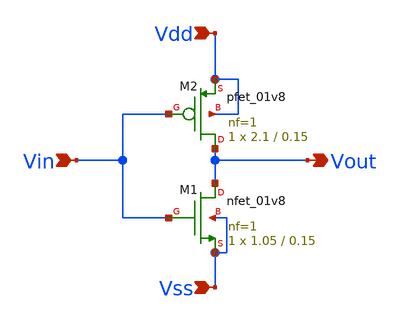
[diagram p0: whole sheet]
** sch_path: trabajosPracticos/tp6/archivosDelProfe/inversor/inversor.sch
**.subckt inversor Vdd Vss Vin Vout
*.ipin Vdd
*.ipin Vss
*.ipin Vin
*.opin Vout
XM2 Vout Vin Vdd Vdd sky130_fd_pr__pfet_01v8 L=0.15 W=2.1 nf=1 ad='int((nf+1)/2) * W/nf * 0.29' as='int((nf+2)/2) * W/nf * 0.29'
+ pd='2*int((nf+1)/2) * (W/nf + 0.29)' ps='2*int((nf+2)/2) * (W/nf + 0.29)' nrd='0.29 / W' nrs='0.29 / W'
+ sa=0 sb=0 sd=0 mult=1 m=1
XM1 Vout Vin Vss Vss sky130_fd_pr__nfet_01v8 L=0.15 W=1.05 nf=1 ad='int((nf+1)/2) * W/nf * 0.29' as='int((nf+2)/2) * W/nf * 0.29'
+ pd='2*int((nf+1)/2) * (W/nf + 0.29)' ps='2*int((nf+2)/2) * (W/nf + 0.29)' nrd='0.29 / W' nrs='0.29 / W'
+ sa=0 sb=0 sd=0 mult=1 m=1
**.ends
.end
